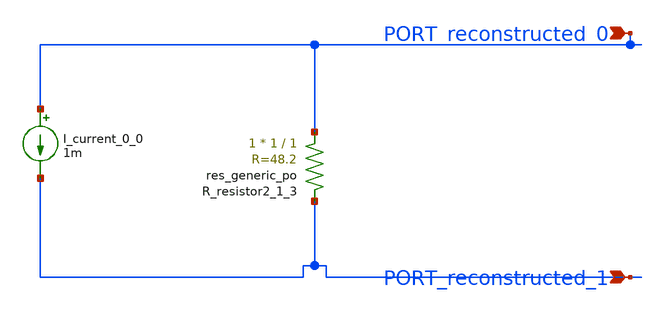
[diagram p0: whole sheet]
** sch_path: schematics/AMSNet/95.sch
**.subckt 95 PORT_reconstructed_1 PORT_reconstructed_0
*.ipin PORT_reconstructed_1
*.ipin PORT_reconstructed_0
I_current_0_0 PORT_reconstructed_0 PORT_reconstructed_1 1m
XR_resistor2_1_3 PORT_reconstructed_0 PORT_reconstructed_1 sky130_fd_pr__res_generic_po W=1 L=1 m=1
**.ends
.end
